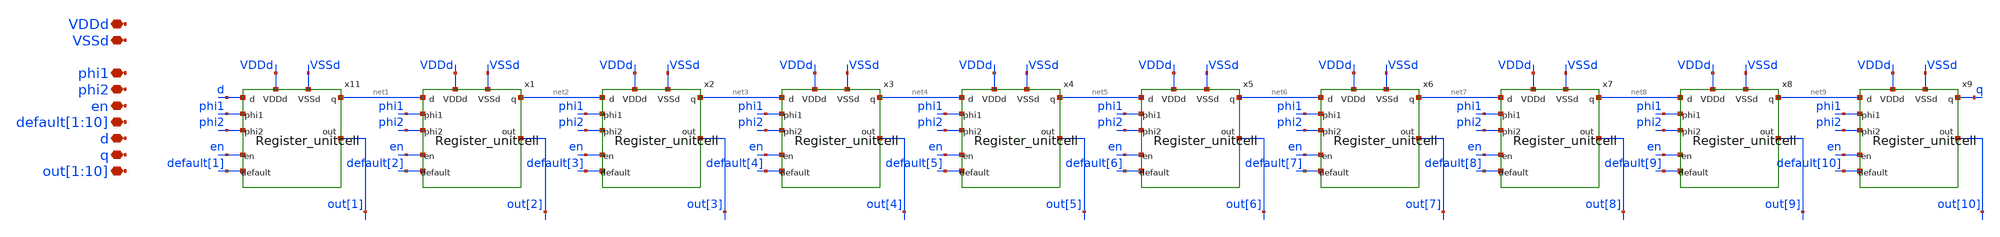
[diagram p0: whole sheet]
** sch_path: designs/libs/qw_core_analog/SRegister_10/SRegister_10.sch
**.subckt SRegister_10 VDDd VSSd phi1 phi2 en
*+ default[1],default[2],default[3],default[4],default[5],default[6],default[7],default[8],default[9],default[10] d q out[1],out[2],out[3],out[4],out[5],out[6],out[7],out[8],out[9],out[10]
*.iopin VDDd
*.iopin VSSd
*.iopin phi1
*.iopin phi2
*.iopin en
*.iopin
*+ default[1],default[2],default[3],default[4],default[5],default[6],default[7],default[8],default[9],default[10]
*.iopin d
*.iopin q
*.iopin out[1],out[2],out[3],out[4],out[5],out[6],out[7],out[8],out[9],out[10]
x11 net1 d phi1 phi2 VDDd VSSd out[1] en default[1] Register_unitcell
x1 net2 net1 phi1 phi2 VDDd VSSd out[2] en default[2] Register_unitcell
x2 net3 net2 phi1 phi2 VDDd VSSd out[3] en default[3] Register_unitcell
x3 net4 net3 phi1 phi2 VDDd VSSd out[4] en default[4] Register_unitcell
x4 net5 net4 phi1 phi2 VDDd VSSd out[5] en default[5] Register_unitcell
x5 net6 net5 phi1 phi2 VDDd VSSd out[6] en default[6] Register_unitcell
x6 net7 net6 phi1 phi2 VDDd VSSd out[7] en default[7] Register_unitcell
x7 net8 net7 phi1 phi2 VDDd VSSd out[8] en default[8] Register_unitcell
x8 net9 net8 phi1 phi2 VDDd VSSd out[9] en default[9] Register_unitcell
x9 q net9 phi1 phi2 VDDd VSSd out[10] en default[10] Register_unitcell
**.ends

* expanding   symbol:  libs/qw_core_analog/Register_unitcell/Register_unitcell.sym # of pins=9
** sym_path: designs/libs/qw_core_analog/Register_unitcell/Register_unitcell.sym
** sch_path: designs/libs/qw_core_analog/Register_unitcell/Register_unitcell.sch
.subckt Register_unitcell q d phi1 phi2 VDDd VSSd out en default
*.iopin phi1
*.iopin phi2
*.iopin d
*.iopin q
*.iopin en
*.iopin default
*.iopin out
*.iopin VDDd
*.iopin VSSd
x4 en VSSd VDDd VSSd VDDd enbar gf180mcu_fd_sc_mcu9t5v0__inv_1
* noconn VDDd
* noconn VSSd
x1 d q phi1 phi2 DFF_2phase_1
x2 q en VSSd VDDd VSSd VDDd or1 gf180mcu_fd_sc_mcu9t5v0__and2_1
x10 or2 or1 VSSd VDDd VSSd VDDd out gf180mcu_fd_sc_mcu9t5v0__or2_1
x3 enbar default VSSd VDDd VSSd VDDd or2 gf180mcu_fd_sc_mcu9t5v0__and2_1
.ends


* expanding   symbol:  libs/qw_core_analog/DFF_2phase_1/DFF_2phase_1.sym # of pins=4
** sym_path: designs/switch_matrix_gf180mcu_9t5v0-main/designs/libs/core_swmatrix/DFF_2phase_1.sym
** sch_path: designs/switch_matrix_gf180mcu_9t5v0-main/designs/libs/core_swmatrix/DFF_2phase_1.sch
.subckt DFF_2phase_1 D Q PHI_1 PHI_2
*.ipin D
*.ipin PHI_1
*.ipin PHI_2
*.opin Q
xmain D PHI_1 out_m VDDd VDDd VSSd VSSd gf180mcu_fd_sc_mcu9t5v0__latq_1
xsecondary out_m PHI_2 Q VDDd VDDd VSSd VSSd gf180mcu_fd_sc_mcu9t5v0__latq_1
.ends

.end
